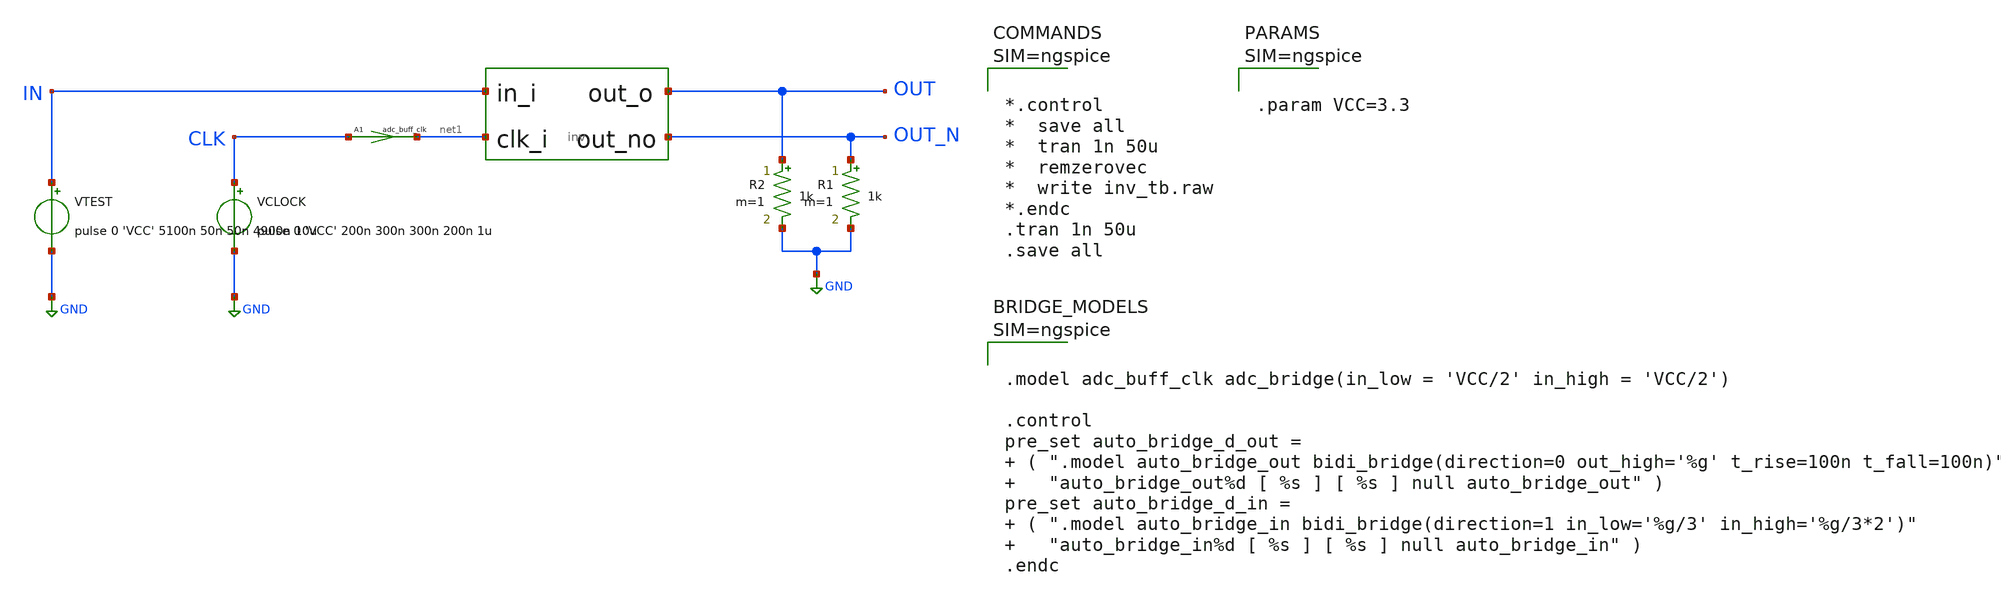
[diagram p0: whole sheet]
** sch_path: designs/inv/inv_tb.sch
**.subckt inv_tb
ADUT [ net1 IN ] [ OUT OUT_N ] dut
VCLOCK CLK GND pulse 0 'VCC' 200n 300n 300n 200n 1u
VTEST IN GND pulse 0 'VCC' 5100n 50n 50n 4900n 10u
R1 OUT_N GND 1k m=1
R2 OUT GND 1k m=1
A1 [ CLK ] [ net1 ] adc_buff_clk
**** begin user architecture code



*.control
*  save all
*  tran 1n 50u
*  remzerovec
*  write inv_tb.raw
*.endc
.tran 1n 50u
.save all






.param VCC=3.3






.model adc_buff_clk adc_bridge(in_low = 'VCC/2' in_high = 'VCC/2')

.control
pre_set auto_bridge_d_out =  ( ".model auto_bridge_out bidi_bridge(direction=0 out_high='%g' t_rise=100n
+ t_fall=100n)"    "auto_bridge_out%d [ %s ] [ %s ] null auto_bridge_out" )
pre_set auto_bridge_d_in =  ( ".model auto_bridge_in bidi_bridge(direction=1 in_low='%g/3' in_high='%g/3*2')"
+    "auto_bridge_in%d [ %s ] [ %s ] null auto_bridge_in" )
.endc



**** end user architecture code
**.ends
.GLOBAL GND
**** begin user architecture code
.model dut d_cosim simulation="ivlng" sim_args=["inv"]
**** end user architecture code
.end
